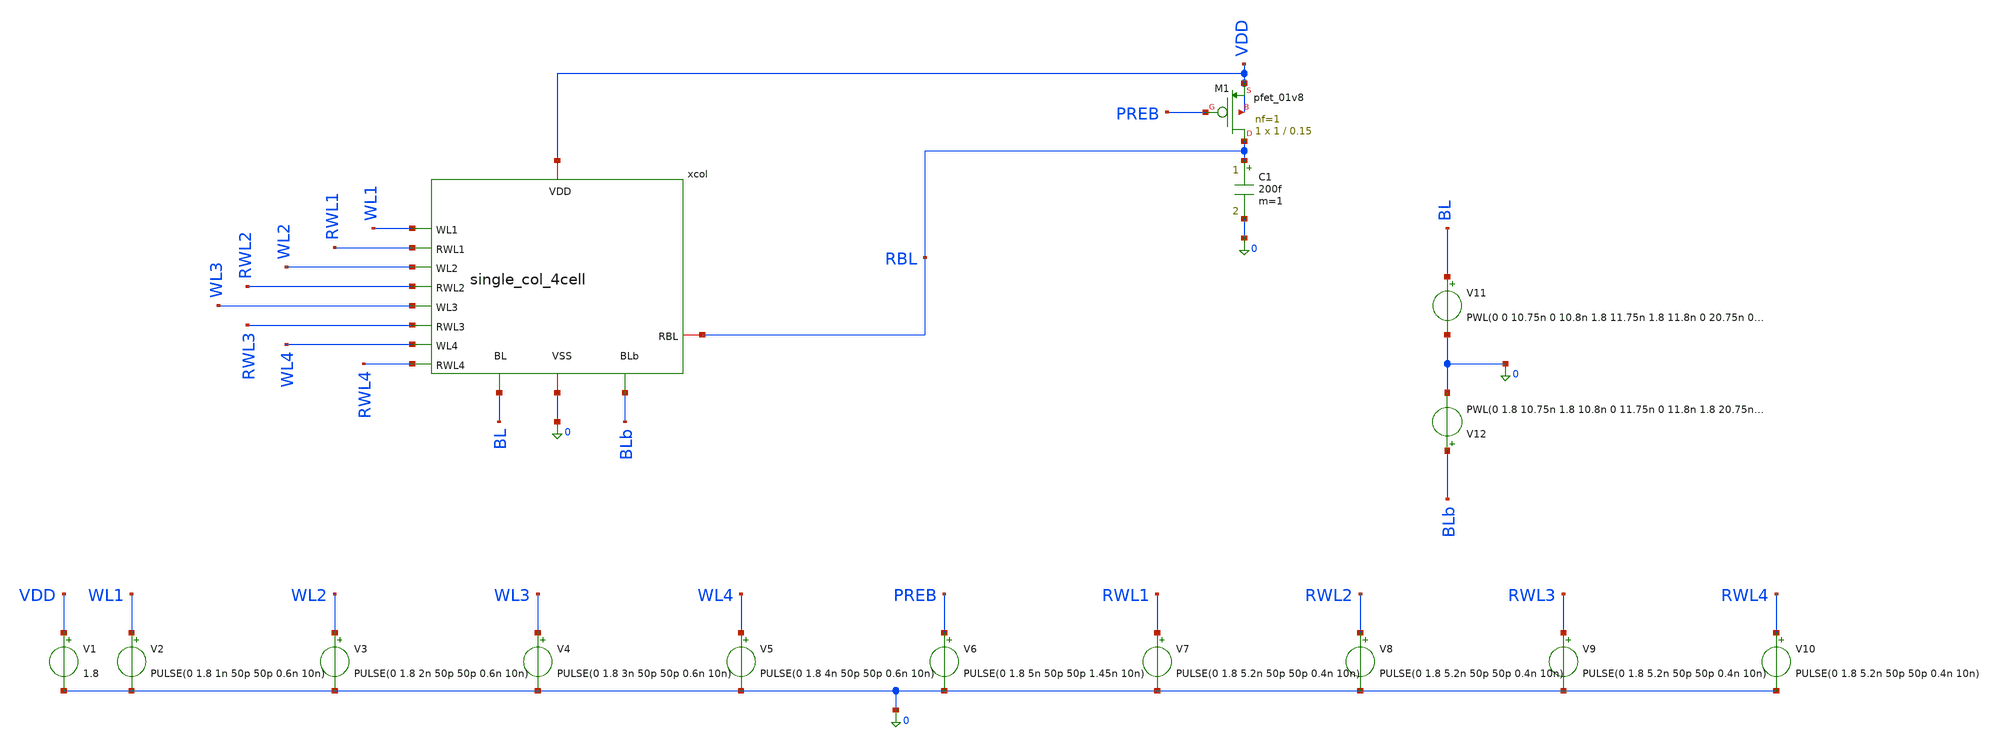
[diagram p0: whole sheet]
** sch_path: schematics/single_col_4cell_tb.sch
**.subckt single_col_4cell_tb
V1 VDD 0 1.8
V2 WL1 0 PULSE(0 1.8 1n 50p 50p 0.6n 10n)
V3 WL2 0 PULSE(0 1.8 2n 50p 50p 0.6n 10n)
V4 WL3 0 PULSE(0 1.8 3n 50p 50p 0.6n 10n)
V5 WL4 0 PULSE(0 1.8 4n 50p 50p 0.6n 10n)
V6 PREB 0 PULSE(0 1.8 5n 50p 50p 1.45n 10n)
V7 RWL1 0 PULSE(0 1.8 5.2n 50p 50p 0.4n 10n)
V8 RWL2 0 PULSE(0 1.8 5.2n 50p 50p 0.4n 10n)
V9 RWL3 0 PULSE(0 1.8 5.2n 50p 50p 0.4n 10n)
V10 RWL4 0 PULSE(0 1.8 5.2n 50p 50p 0.4n 10n)
V11 BL 0 PWL(0 0 10.75n 0 10.8n 1.8 11.75n 1.8 11.8n 0 20.75n 0 20.8n 1.8 22.75n 1.8 22.8n 0 30.75n
+ 0 30.8n 1.8 33.75n 1.8 33.8n 0 40.75n 0 40.8n 1.8 50.75n 1.8 50.8n 0 51.75n 0 51.8n 1.8 52.75n 1.8
+ 52.8n 0 53.75n 0 53.8n 1.8 60n 1.8)
V12 BLb 0 PWL(0 1.8 10.75n 1.8 10.8n 0 11.75n 0 11.8n 1.8 20.75n 1.8 20.8n 0 22.75n 0 22.8n 1.8
+ 30.75n 1.8 30.8n 0 33.75n 0 33.8n 1.8 40.75n 1.8 40.8n 0 50.75n 0 50.8n 1.8 51.75n 1.8 51.8n 0 52.75n 0
+ 52.8n 1.8 53.75n 1.8 53.8n 0 60n 0)
C1 RBL 0 200f m=1
XM1 RBL PREB VDD VDD sky130_fd_pr__pfet_01v8 L=0.15 W=1 nf=1 ad='int((1 + 1)/2) * 1 / 1 * 0.29' as='int((1 + 2)/2) * 1 / 1 * 0.29'
+ pd='2*int((1 + 1)/2) * (1 / 1 + 0.29)' ps='2*int((1 + 2)/2) * (1 / 1 + 0.29)' nrd='0.29 / 1 ' nrs='0.29 / 1 '
+ sa=0 sb=0 sd=0 mult=1 m=1
xcol WL1 VDD BL BLb RBL RWL1 WL2 RWL2 WL3 RWL3 WL4 RWL4 0 single_col_4cell
**** begin user architecture code


.lib /usr/local/share/pdk/sky130A/libs.tech/ngspice/sky130.lib.spice tt
.ic v(xcol.x1.q)=0 v(xcol.x1.qb)=1.8 v(xcol.x2.q)=0 v(xcol.x2.qb)=1.8 v(xcol.x3.q)=0
+ v(xcol.x3.qb)=1.8 v(xcol.x4.q)=0 v(xcol.x4.qb)=1.8 v(rbl)=1.8
.tran 5p 60n uic
.control
run
meas tran p0a FIND v(rbl) AT=5.65n
meas tran p0b FIND v(rbl) AT=5.9n
meas tran p1a FIND v(rbl) AT=15.65n
meas tran p1b FIND v(rbl) AT=15.9n
meas tran p2a FIND v(rbl) AT=25.65n
meas tran p2b FIND v(rbl) AT=25.9n
meas tran p3a FIND v(rbl) AT=35.65n
meas tran p3b FIND v(rbl) AT=35.9n
meas tran p4a FIND v(rbl) AT=45.65n
meas tran p4b FIND v(rbl) AT=45.9n
meas tran p5a FIND v(rbl) AT=55.65n
meas tran p5b FIND v(rbl) AT=55.9n
plot v(xcol.x1.q)+14 v(xcol.x2.q)+12 v(xcol.x3.q)+10 v(xcol.x4.q)+8 v(rwl1)+6 v(preb)+4 v(rbl)
plot v(rbl)
.endc


**** end user architecture code
**.ends
.end
